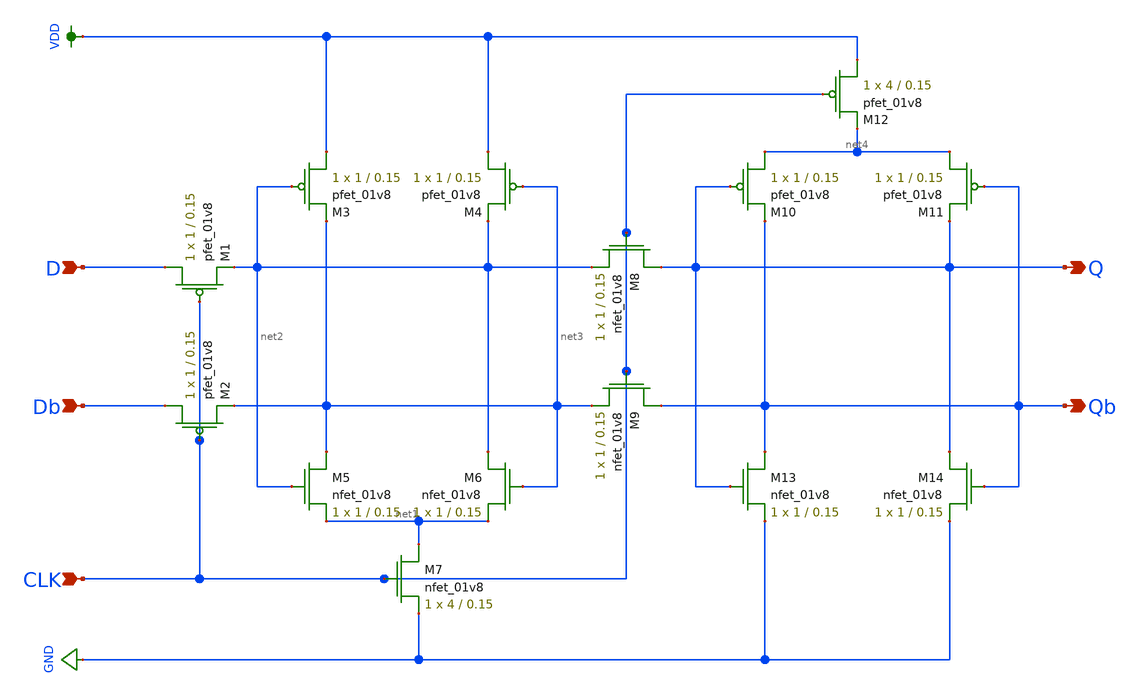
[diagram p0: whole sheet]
** sch_path: simulation/shift_register/andrew_mp2_files/d_flipflop/d_flipflop.sch
**.subckt d_flipflop D CLK Q Qb Db
*.ipin D
*.ipin CLK
*.opin Q
*.opin Qb
*.ipin Db
XM1 D CLK net2 VP sky130_fd_pr__pfet_01v8 L=0.15 W=1 nf=1 ad='int((nf+1)/2) * W/nf * 0.29' as='int((nf+2)/2) * W/nf * 0.29'
+ pd='2*int((nf+1)/2) * (W/nf + 0.29)' ps='2*int((nf+2)/2) * (W/nf + 0.29)' nrd='0.29 / W' nrs='0.29 / W'
+ sa=0 sb=0 sd=0 mult=1 m=1
XM2 Db CLK net3 VP sky130_fd_pr__pfet_01v8 L=0.15 W=1 nf=1 ad='int((nf+1)/2) * W/nf * 0.29' as='int((nf+2)/2) * W/nf * 0.29'
+ pd='2*int((nf+1)/2) * (W/nf + 0.29)' ps='2*int((nf+2)/2) * (W/nf + 0.29)' nrd='0.29 / W' nrs='0.29 / W'
+ sa=0 sb=0 sd=0 mult=1 m=1
XM3 VDD net2 net3 VP sky130_fd_pr__pfet_01v8 L=0.15 W=1 nf=1 ad='int((nf+1)/2) * W/nf * 0.29' as='int((nf+2)/2) * W/nf * 0.29'
+ pd='2*int((nf+1)/2) * (W/nf + 0.29)' ps='2*int((nf+2)/2) * (W/nf + 0.29)' nrd='0.29 / W' nrs='0.29 / W'
+ sa=0 sb=0 sd=0 mult=1 m=1
XM5 net3 net2 net1 VN sky130_fd_pr__nfet_01v8 L=0.15 W=1 nf=1 ad='int((nf+1)/2) * W/nf * 0.29' as='int((nf+2)/2) * W/nf * 0.29'
+ pd='2*int((nf+1)/2) * (W/nf + 0.29)' ps='2*int((nf+2)/2) * (W/nf + 0.29)' nrd='0.29 / W' nrs='0.29 / W'
+ sa=0 sb=0 sd=0 mult=1 m=1
XM7 net1 CLK GND VN sky130_fd_pr__nfet_01v8 L=0.15 W=4 nf=1 ad='int((nf+1)/2) * W/nf * 0.29' as='int((nf+2)/2) * W/nf * 0.29'
+ pd='2*int((nf+1)/2) * (W/nf + 0.29)' ps='2*int((nf+2)/2) * (W/nf + 0.29)' nrd='0.29 / W' nrs='0.29 / W'
+ sa=0 sb=0 sd=0 mult=1 m=1
XM8 Q CLK net2 VN sky130_fd_pr__nfet_01v8 L=0.15 W=1 nf=1 ad='int((nf+1)/2) * W/nf * 0.29' as='int((nf+2)/2) * W/nf * 0.29'
+ pd='2*int((nf+1)/2) * (W/nf + 0.29)' ps='2*int((nf+2)/2) * (W/nf + 0.29)' nrd='0.29 / W' nrs='0.29 / W'
+ sa=0 sb=0 sd=0 mult=1 m=1
XM9 Qb CLK net3 VN sky130_fd_pr__nfet_01v8 L=0.15 W=1 nf=1 ad='int((nf+1)/2) * W/nf * 0.29' as='int((nf+2)/2) * W/nf * 0.29'
+ pd='2*int((nf+1)/2) * (W/nf + 0.29)' ps='2*int((nf+2)/2) * (W/nf + 0.29)' nrd='0.29 / W' nrs='0.29 / W'
+ sa=0 sb=0 sd=0 mult=1 m=1
XM10 net4 Q Qb VP sky130_fd_pr__pfet_01v8 L=0.15 W=1 nf=1 ad='int((nf+1)/2) * W/nf * 0.29' as='int((nf+2)/2) * W/nf * 0.29'
+ pd='2*int((nf+1)/2) * (W/nf + 0.29)' ps='2*int((nf+2)/2) * (W/nf + 0.29)' nrd='0.29 / W' nrs='0.29 / W'
+ sa=0 sb=0 sd=0 mult=1 m=1
XM11 net4 Qb Q VP sky130_fd_pr__pfet_01v8 L=0.15 W=1 nf=1 ad='int((nf+1)/2) * W/nf * 0.29' as='int((nf+2)/2) * W/nf * 0.29'
+ pd='2*int((nf+1)/2) * (W/nf + 0.29)' ps='2*int((nf+2)/2) * (W/nf + 0.29)' nrd='0.29 / W' nrs='0.29 / W'
+ sa=0 sb=0 sd=0 mult=1 m=1
XM12 VDD CLK net4 VP sky130_fd_pr__pfet_01v8 L=0.15 W=4 nf=1 ad='int((nf+1)/2) * W/nf * 0.29' as='int((nf+2)/2) * W/nf * 0.29'
+ pd='2*int((nf+1)/2) * (W/nf + 0.29)' ps='2*int((nf+2)/2) * (W/nf + 0.29)' nrd='0.29 / W' nrs='0.29 / W'
+ sa=0 sb=0 sd=0 mult=1 m=1
XM13 Qb Q GND VN sky130_fd_pr__nfet_01v8 L=0.15 W=1 nf=1 ad='int((nf+1)/2) * W/nf * 0.29' as='int((nf+2)/2) * W/nf * 0.29'
+ pd='2*int((nf+1)/2) * (W/nf + 0.29)' ps='2*int((nf+2)/2) * (W/nf + 0.29)' nrd='0.29 / W' nrs='0.29 / W'
+ sa=0 sb=0 sd=0 mult=1 m=1
XM14 Q Qb GND VN sky130_fd_pr__nfet_01v8 L=0.15 W=1 nf=1 ad='int((nf+1)/2) * W/nf * 0.29' as='int((nf+2)/2) * W/nf * 0.29'
+ pd='2*int((nf+1)/2) * (W/nf + 0.29)' ps='2*int((nf+2)/2) * (W/nf + 0.29)' nrd='0.29 / W' nrs='0.29 / W'
+ sa=0 sb=0 sd=0 mult=1 m=1
XM4 VDD net3 net2 VP sky130_fd_pr__pfet_01v8 L=0.15 W=1 nf=1 ad='int((nf+1)/2) * W/nf * 0.29' as='int((nf+2)/2) * W/nf * 0.29'
+ pd='2*int((nf+1)/2) * (W/nf + 0.29)' ps='2*int((nf+2)/2) * (W/nf + 0.29)' nrd='0.29 / W' nrs='0.29 / W'
+ sa=0 sb=0 sd=0 mult=1 m=1
XM6 net2 net3 net1 VN sky130_fd_pr__nfet_01v8 L=0.15 W=1 nf=1 ad='int((nf+1)/2) * W/nf * 0.29' as='int((nf+2)/2) * W/nf * 0.29'
+ pd='2*int((nf+1)/2) * (W/nf + 0.29)' ps='2*int((nf+2)/2) * (W/nf + 0.29)' nrd='0.29 / W' nrs='0.29 / W'
+ sa=0 sb=0 sd=0 mult=1 m=1
**.ends
.GLOBAL VDD
.GLOBAL GND
.end
